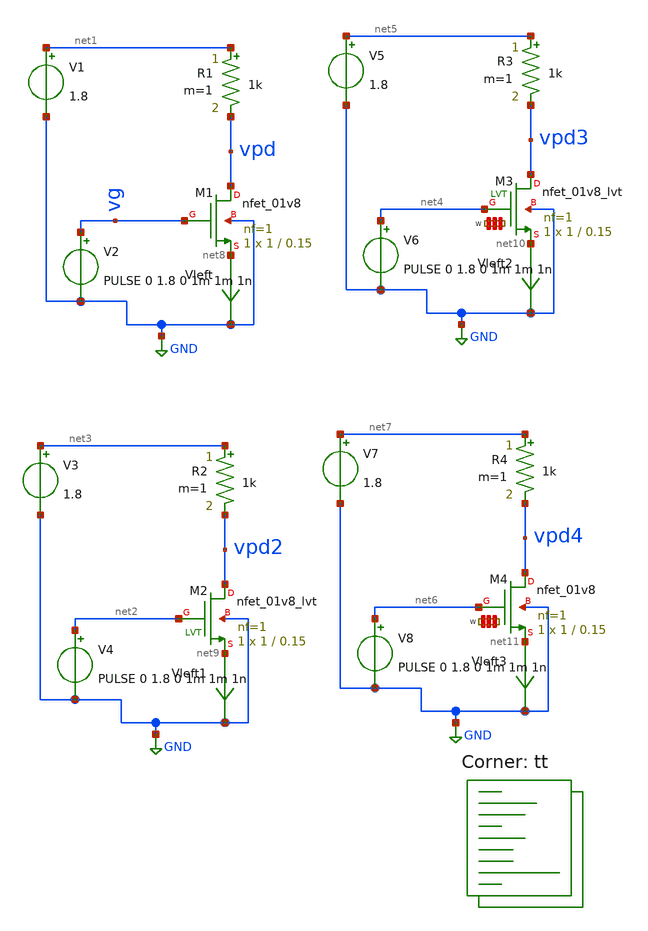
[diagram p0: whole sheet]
** sch_path: Schematics/mos_resistors/nmos_resistor_var.sch
**.subckt nmos_resistor_var
V1 net1 GND 1.8
.save i(v1)
R1 net1 vpd 1k m=1
V2 vg GND PULSE 0 1.8 0 1m 1m 1n
.save i(v2)
Vleft net8 GND 0
.save i(vleft)
XM1 vpd vg net8 GND sky130_fd_pr__nfet_01v8 L=0.15 W=1 nf=1 ad='int((nf+1)/2) * W/nf * 0.29' as='int((nf+2)/2) * W/nf * 0.29'
+ pd='2*int((nf+1)/2) * (W/nf + 0.29)' ps='2*int((nf+2)/2) * (W/nf + 0.29)' nrd='0.29 / W' nrs='0.29 / W'
+ sa=0 sb=0 sd=0 mult=1 m=1
V3 net3 GND 1.8
.save i(v3)
R2 net3 vpd2 1k m=1
V4 net2 GND PULSE 0 1.8 0 1m 1m 1n
.save i(v4)
Vleft1 net9 GND 0
.save i(vleft1)
XM2 vpd2 net2 net9 GND sky130_fd_pr__nfet_01v8_lvt L=0.15 W=1 nf=1 ad='int((nf+1)/2) * W/nf * 0.29' as='int((nf+2)/2) * W/nf * 0.29'
+ pd='2*int((nf+1)/2) * (W/nf + 0.29)' ps='2*int((nf+2)/2) * (W/nf + 0.29)' nrd='0.29 / W' nrs='0.29 / W'
+ sa=0 sb=0 sd=0 mult=1 m=1
V5 net5 GND 1.8
.save i(v5)
R3 net5 vpd3 1k m=1
V6 net4 GND PULSE 0 1.8 0 1m 1m 1n
.save i(v6)
Vleft2 net10 GND 0
.save i(vleft2)
V7 net7 GND 1.8
.save i(v7)
R4 net7 vpd4 1k m=1
V8 net6 GND PULSE 0 1.8 0 1m 1m 1n
.save i(v8)
Vleft3 net11 GND 0
.save i(vleft3)
XM3 vpd3 net4 net10 GND sky130_fd_pr__nfet_01v8_lvt L=0.15 W='1 * 1 ' nf=1 ad='int((nf+1)/2) * W / nf * 0.29'
+ as='int((nf+2)/2) * W / nf * 0.29' pd='2*int((nf+1)/2) * (W / nf + 0.29)' ps='2*int((nf+2)/2) * (W / nf + 0.29)'
+ nrd='0.29 / W ' nrs='0.29 / W ' sa=0 sb=0 sd=0 mult=1 m=1
XM4 vpd4 net6 net11 GND sky130_fd_pr__nfet_01v8 L=0.15 W='1 * 1 ' nf=1 ad='int((nf+1)/2) * W / nf * 0.29'
+ as='int((nf+2)/2) * W / nf * 0.29' pd='2*int((nf+1)/2) * (W / nf + 0.29)' ps='2*int((nf+2)/2) * (W / nf + 0.29)'
+ nrd='0.29 / W ' nrs='0.29 / W ' sa=0 sb=0 sd=0 mult=1 m=1
**** begin user architecture code
.lib $::SKYWATER_MODELS/sky130.lib.spice tt
**** end user architecture code
**.ends
.GLOBAL GND
**** begin user architecture code

*.options savecurrents
.tran 10u 2m
.save all
.control
	run
	write nmos_resistor_var.raw
.endc


**** end user architecture code
.end
